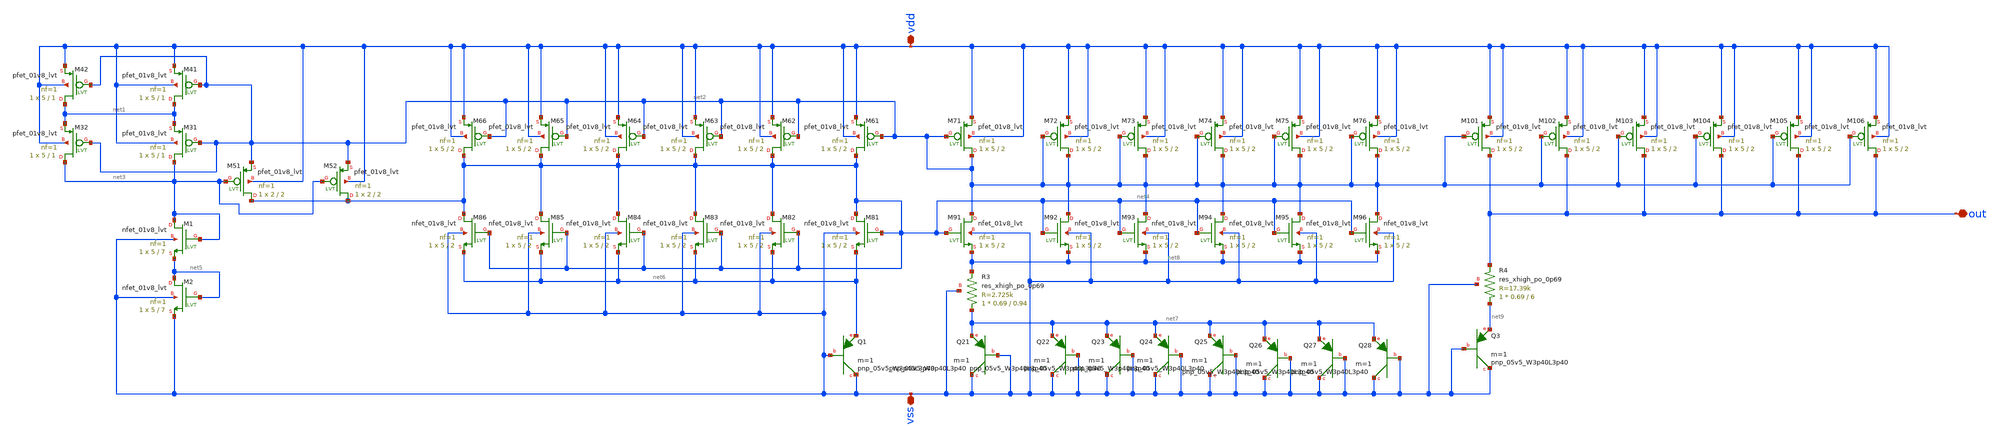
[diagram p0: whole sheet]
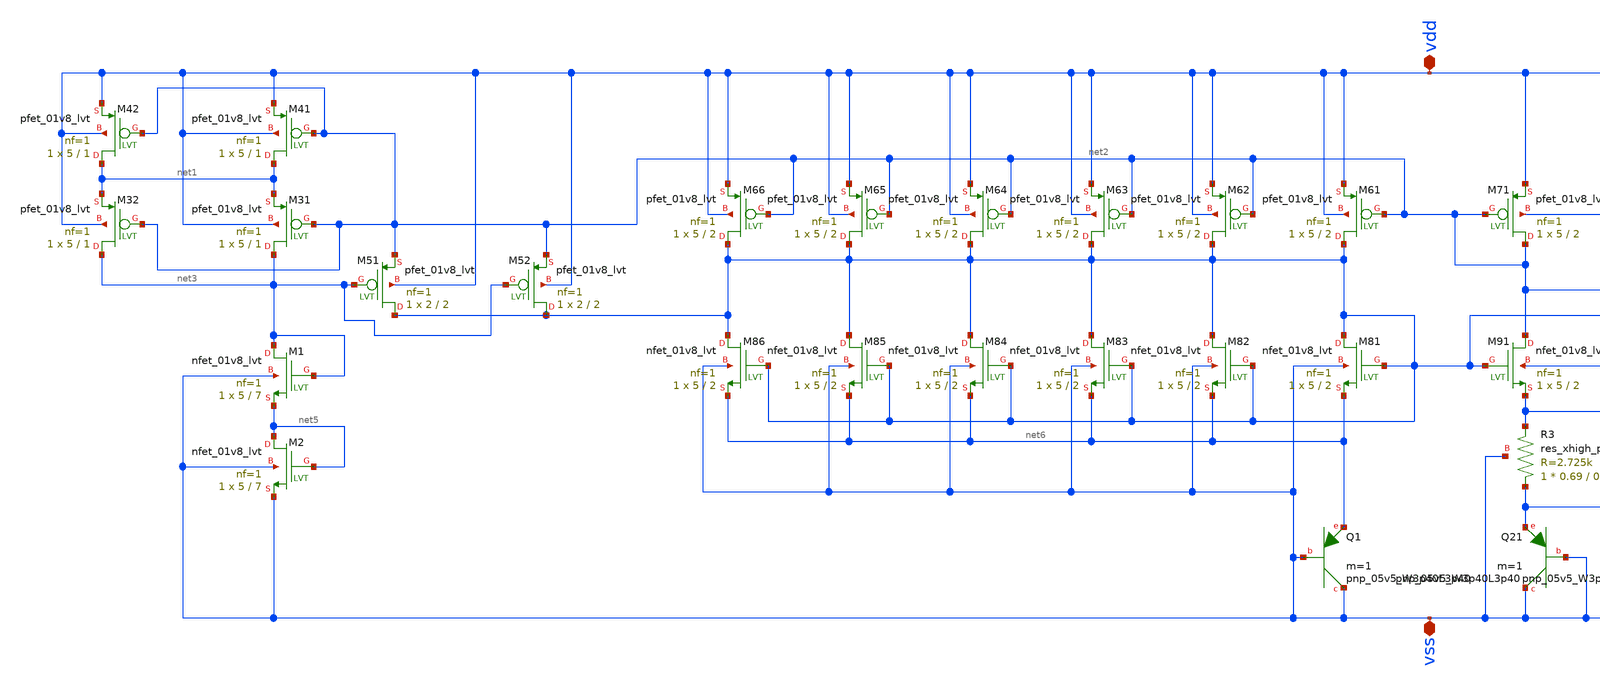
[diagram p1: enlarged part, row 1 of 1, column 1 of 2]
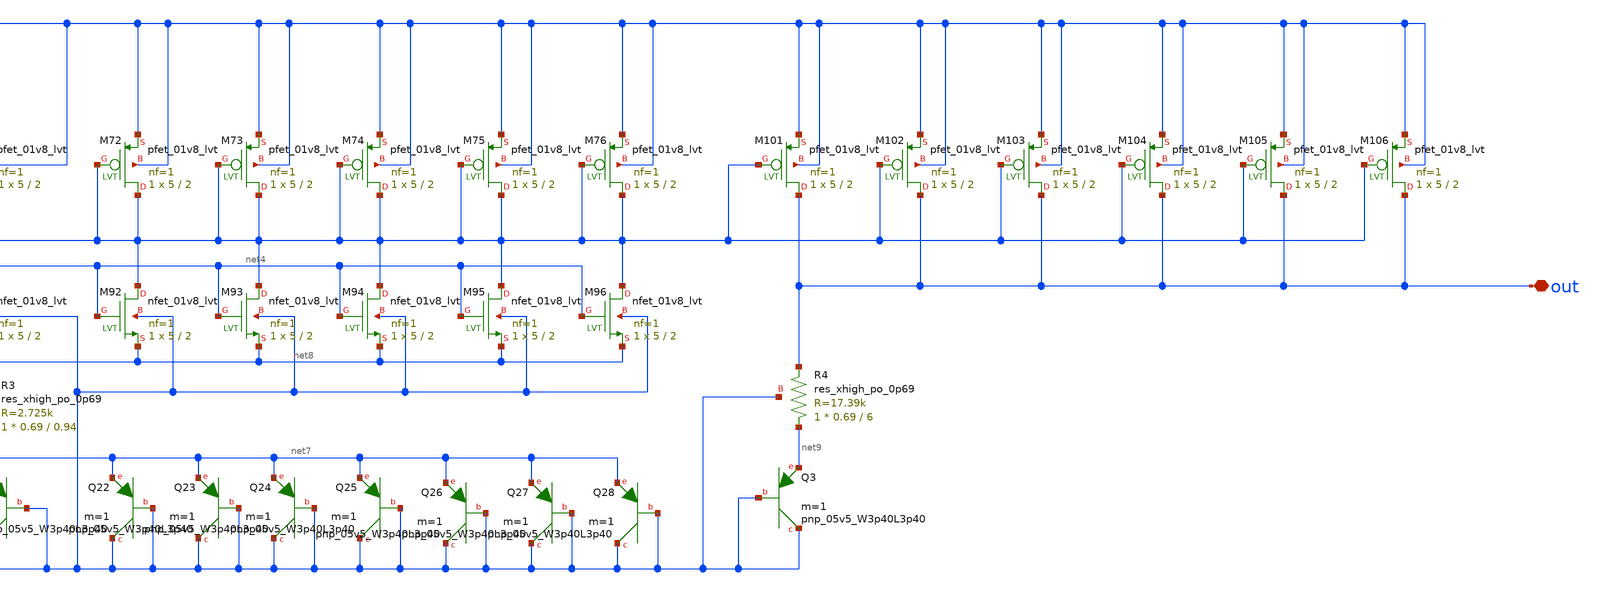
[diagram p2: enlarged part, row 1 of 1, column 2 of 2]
** sch_path: XSCHEM/For_Layout/BGR_lvt.sch
**.subckt BGR_lvt vdd vss out
*.iopin vdd
*.iopin vss
*.iopin out
XM1 net3 net3 net5 vss sky130_fd_pr__nfet_01v8_lvt L=7 W=5 nf=1 ad='int((nf+1)/2) * W/nf * 0.29' as='int((nf+2)/2) * W/nf * 0.29'
+ pd='2*int((nf+1)/2) * (W/nf + 0.29)' ps='2*int((nf+2)/2) * (W/nf + 0.29)' nrd='0.29 / W' nrs='0.29 / W'
+ sa=0 sb=0 sd=0 mult=1 m=1
XM2 net5 net5 vss vss sky130_fd_pr__nfet_01v8_lvt L=7 W=5 nf=1 ad='int((nf+1)/2) * W/nf * 0.29' as='int((nf+2)/2) * W/nf * 0.29'
+ pd='2*int((nf+1)/2) * (W/nf + 0.29)' ps='2*int((nf+2)/2) * (W/nf + 0.29)' nrd='0.29 / W' nrs='0.29 / W'
+ sa=0 sb=0 sd=0 mult=1 m=1
XM31 net3 net2 net1 vdd sky130_fd_pr__pfet_01v8_lvt L=1 W=5 nf=1 ad='int((nf+1)/2) * W/nf * 0.29' as='int((nf+2)/2) * W/nf * 0.29'
+ pd='2*int((nf+1)/2) * (W/nf + 0.29)' ps='2*int((nf+2)/2) * (W/nf + 0.29)' nrd='0.29 / W' nrs='0.29 / W'
+ sa=0 sb=0 sd=0 mult=1 m=1
XM41 net1 net2 vdd vdd sky130_fd_pr__pfet_01v8_lvt L=1 W=5 nf=1 ad='int((nf+1)/2) * W/nf * 0.29' as='int((nf+2)/2) * W/nf * 0.29'
+ pd='2*int((nf+1)/2) * (W/nf + 0.29)' ps='2*int((nf+2)/2) * (W/nf + 0.29)' nrd='0.29 / W' nrs='0.29 / W'
+ sa=0 sb=0 sd=0 mult=1 m=1
XM51 net4 net3 net2 vdd sky130_fd_pr__pfet_01v8_lvt L=2 W=2 nf=1 ad='int((nf+1)/2) * W/nf * 0.29' as='int((nf+2)/2) * W/nf * 0.29'
+ pd='2*int((nf+1)/2) * (W/nf + 0.29)' ps='2*int((nf+2)/2) * (W/nf + 0.29)' nrd='0.29 / W' nrs='0.29 / W'
+ sa=0 sb=0 sd=0 mult=1 m=1
XM61 net4 net2 vdd vdd sky130_fd_pr__pfet_01v8_lvt L=2 W=5 nf=1 ad='int((nf+1)/2) * W/nf * 0.29' as='int((nf+2)/2) * W/nf * 0.29'
+ pd='2*int((nf+1)/2) * (W/nf + 0.29)' ps='2*int((nf+2)/2) * (W/nf + 0.29)' nrd='0.29 / W' nrs='0.29 / W'
+ sa=0 sb=0 sd=0 mult=1 m=1
XM71 net2 net2 vdd vdd sky130_fd_pr__pfet_01v8_lvt L=2 W=5 nf=1 ad='int((nf+1)/2) * W/nf * 0.29' as='int((nf+2)/2) * W/nf * 0.29'
+ pd='2*int((nf+1)/2) * (W/nf + 0.29)' ps='2*int((nf+2)/2) * (W/nf + 0.29)' nrd='0.29 / W' nrs='0.29 / W'
+ sa=0 sb=0 sd=0 mult=1 m=1
XM81 net4 net4 net6 vss sky130_fd_pr__nfet_01v8_lvt L=2 W=5 nf=1 ad='int((nf+1)/2) * W/nf * 0.29' as='int((nf+2)/2) * W/nf * 0.29'
+ pd='2*int((nf+1)/2) * (W/nf + 0.29)' ps='2*int((nf+2)/2) * (W/nf + 0.29)' nrd='0.29 / W' nrs='0.29 / W'
+ sa=0 sb=0 sd=0 mult=1 m=1
XM91 net2 net4 net8 vss sky130_fd_pr__nfet_01v8_lvt L=2 W=5 nf=1 ad='int((nf+1)/2) * W/nf * 0.29' as='int((nf+2)/2) * W/nf * 0.29'
+ pd='2*int((nf+1)/2) * (W/nf + 0.29)' ps='2*int((nf+2)/2) * (W/nf + 0.29)' nrd='0.29 / W' nrs='0.29 / W'
+ sa=0 sb=0 sd=0 mult=1 m=1
XQ1 vss vss net6 sky130_fd_pr__pnp_05v5_W3p40L3p40 m=1
XQ21 vss vss net7 sky130_fd_pr__pnp_05v5_W3p40L3p40 m=1
XM101 out net2 vdd vdd sky130_fd_pr__pfet_01v8_lvt L=2 W=5 nf=1 ad='int((nf+1)/2) * W/nf * 0.29' as='int((nf+2)/2) * W/nf * 0.29'
+ pd='2*int((nf+1)/2) * (W/nf + 0.29)' ps='2*int((nf+2)/2) * (W/nf + 0.29)' nrd='0.29 / W' nrs='0.29 / W'
+ sa=0 sb=0 sd=0 mult=1 m=1
XQ3 vss vss net9 sky130_fd_pr__pnp_05v5_W3p40L3p40 m=1
XR3 net7 net8 vss sky130_fd_pr__res_xhigh_po_0p69 L=0.94 mult=1 m=1
XR4 net9 out vss sky130_fd_pr__res_xhigh_po_0p69 L=6 mult=1 m=1
XM42 net1 net2 vdd vdd sky130_fd_pr__pfet_01v8_lvt L=1 W=5 nf=1 ad='int((nf+1)/2) * W/nf * 0.29' as='int((nf+2)/2) * W/nf * 0.29'
+ pd='2*int((nf+1)/2) * (W/nf + 0.29)' ps='2*int((nf+2)/2) * (W/nf + 0.29)' nrd='0.29 / W' nrs='0.29 / W'
+ sa=0 sb=0 sd=0 mult=1 m=1
XM32 net3 net2 net1 vdd sky130_fd_pr__pfet_01v8_lvt L=1 W=5 nf=1 ad='int((nf+1)/2) * W/nf * 0.29' as='int((nf+2)/2) * W/nf * 0.29'
+ pd='2*int((nf+1)/2) * (W/nf + 0.29)' ps='2*int((nf+2)/2) * (W/nf + 0.29)' nrd='0.29 / W' nrs='0.29 / W'
+ sa=0 sb=0 sd=0 mult=1 m=1
XM52 net4 net3 net2 vdd sky130_fd_pr__pfet_01v8_lvt L=2 W=2 nf=1 ad='int((nf+1)/2) * W/nf * 0.29' as='int((nf+2)/2) * W/nf * 0.29'
+ pd='2*int((nf+1)/2) * (W/nf + 0.29)' ps='2*int((nf+2)/2) * (W/nf + 0.29)' nrd='0.29 / W' nrs='0.29 / W'
+ sa=0 sb=0 sd=0 mult=1 m=1
XM62 net4 net2 vdd vdd sky130_fd_pr__pfet_01v8_lvt L=2 W=5 nf=1 ad='int((nf+1)/2) * W/nf * 0.29' as='int((nf+2)/2) * W/nf * 0.29'
+ pd='2*int((nf+1)/2) * (W/nf + 0.29)' ps='2*int((nf+2)/2) * (W/nf + 0.29)' nrd='0.29 / W' nrs='0.29 / W'
+ sa=0 sb=0 sd=0 mult=1 m=1
XM63 net4 net2 vdd vdd sky130_fd_pr__pfet_01v8_lvt L=2 W=5 nf=1 ad='int((nf+1)/2) * W/nf * 0.29' as='int((nf+2)/2) * W/nf * 0.29'
+ pd='2*int((nf+1)/2) * (W/nf + 0.29)' ps='2*int((nf+2)/2) * (W/nf + 0.29)' nrd='0.29 / W' nrs='0.29 / W'
+ sa=0 sb=0 sd=0 mult=1 m=1
XM64 net4 net2 vdd vdd sky130_fd_pr__pfet_01v8_lvt L=2 W=5 nf=1 ad='int((nf+1)/2) * W/nf * 0.29' as='int((nf+2)/2) * W/nf * 0.29'
+ pd='2*int((nf+1)/2) * (W/nf + 0.29)' ps='2*int((nf+2)/2) * (W/nf + 0.29)' nrd='0.29 / W' nrs='0.29 / W'
+ sa=0 sb=0 sd=0 mult=1 m=1
XM65 net4 net2 vdd vdd sky130_fd_pr__pfet_01v8_lvt L=2 W=5 nf=1 ad='int((nf+1)/2) * W/nf * 0.29' as='int((nf+2)/2) * W/nf * 0.29'
+ pd='2*int((nf+1)/2) * (W/nf + 0.29)' ps='2*int((nf+2)/2) * (W/nf + 0.29)' nrd='0.29 / W' nrs='0.29 / W'
+ sa=0 sb=0 sd=0 mult=1 m=1
XM66 net4 net2 vdd vdd sky130_fd_pr__pfet_01v8_lvt L=2 W=5 nf=1 ad='int((nf+1)/2) * W/nf * 0.29' as='int((nf+2)/2) * W/nf * 0.29'
+ pd='2*int((nf+1)/2) * (W/nf + 0.29)' ps='2*int((nf+2)/2) * (W/nf + 0.29)' nrd='0.29 / W' nrs='0.29 / W'
+ sa=0 sb=0 sd=0 mult=1 m=1
XM82 net4 net4 net6 vss sky130_fd_pr__nfet_01v8_lvt L=2 W=5 nf=1 ad='int((nf+1)/2) * W/nf * 0.29' as='int((nf+2)/2) * W/nf * 0.29'
+ pd='2*int((nf+1)/2) * (W/nf + 0.29)' ps='2*int((nf+2)/2) * (W/nf + 0.29)' nrd='0.29 / W' nrs='0.29 / W'
+ sa=0 sb=0 sd=0 mult=1 m=1
XM83 net4 net4 net6 vss sky130_fd_pr__nfet_01v8_lvt L=2 W=5 nf=1 ad='int((nf+1)/2) * W/nf * 0.29' as='int((nf+2)/2) * W/nf * 0.29'
+ pd='2*int((nf+1)/2) * (W/nf + 0.29)' ps='2*int((nf+2)/2) * (W/nf + 0.29)' nrd='0.29 / W' nrs='0.29 / W'
+ sa=0 sb=0 sd=0 mult=1 m=1
XM84 net4 net4 net6 vss sky130_fd_pr__nfet_01v8_lvt L=2 W=5 nf=1 ad='int((nf+1)/2) * W/nf * 0.29' as='int((nf+2)/2) * W/nf * 0.29'
+ pd='2*int((nf+1)/2) * (W/nf + 0.29)' ps='2*int((nf+2)/2) * (W/nf + 0.29)' nrd='0.29 / W' nrs='0.29 / W'
+ sa=0 sb=0 sd=0 mult=1 m=1
XM85 net4 net4 net6 vss sky130_fd_pr__nfet_01v8_lvt L=2 W=5 nf=1 ad='int((nf+1)/2) * W/nf * 0.29' as='int((nf+2)/2) * W/nf * 0.29'
+ pd='2*int((nf+1)/2) * (W/nf + 0.29)' ps='2*int((nf+2)/2) * (W/nf + 0.29)' nrd='0.29 / W' nrs='0.29 / W'
+ sa=0 sb=0 sd=0 mult=1 m=1
XM86 net4 net4 net6 vss sky130_fd_pr__nfet_01v8_lvt L=2 W=5 nf=1 ad='int((nf+1)/2) * W/nf * 0.29' as='int((nf+2)/2) * W/nf * 0.29'
+ pd='2*int((nf+1)/2) * (W/nf + 0.29)' ps='2*int((nf+2)/2) * (W/nf + 0.29)' nrd='0.29 / W' nrs='0.29 / W'
+ sa=0 sb=0 sd=0 mult=1 m=1
XM72 net2 net2 vdd vdd sky130_fd_pr__pfet_01v8_lvt L=2 W=5 nf=1 ad='int((nf+1)/2) * W/nf * 0.29' as='int((nf+2)/2) * W/nf * 0.29'
+ pd='2*int((nf+1)/2) * (W/nf + 0.29)' ps='2*int((nf+2)/2) * (W/nf + 0.29)' nrd='0.29 / W' nrs='0.29 / W'
+ sa=0 sb=0 sd=0 mult=1 m=1
XM73 net2 net2 vdd vdd sky130_fd_pr__pfet_01v8_lvt L=2 W=5 nf=1 ad='int((nf+1)/2) * W/nf * 0.29' as='int((nf+2)/2) * W/nf * 0.29'
+ pd='2*int((nf+1)/2) * (W/nf + 0.29)' ps='2*int((nf+2)/2) * (W/nf + 0.29)' nrd='0.29 / W' nrs='0.29 / W'
+ sa=0 sb=0 sd=0 mult=1 m=1
XM74 net2 net2 vdd vdd sky130_fd_pr__pfet_01v8_lvt L=2 W=5 nf=1 ad='int((nf+1)/2) * W/nf * 0.29' as='int((nf+2)/2) * W/nf * 0.29'
+ pd='2*int((nf+1)/2) * (W/nf + 0.29)' ps='2*int((nf+2)/2) * (W/nf + 0.29)' nrd='0.29 / W' nrs='0.29 / W'
+ sa=0 sb=0 sd=0 mult=1 m=1
XM75 net2 net2 vdd vdd sky130_fd_pr__pfet_01v8_lvt L=2 W=5 nf=1 ad='int((nf+1)/2) * W/nf * 0.29' as='int((nf+2)/2) * W/nf * 0.29'
+ pd='2*int((nf+1)/2) * (W/nf + 0.29)' ps='2*int((nf+2)/2) * (W/nf + 0.29)' nrd='0.29 / W' nrs='0.29 / W'
+ sa=0 sb=0 sd=0 mult=1 m=1
XM76 net2 net2 vdd vdd sky130_fd_pr__pfet_01v8_lvt L=2 W=5 nf=1 ad='int((nf+1)/2) * W/nf * 0.29' as='int((nf+2)/2) * W/nf * 0.29'
+ pd='2*int((nf+1)/2) * (W/nf + 0.29)' ps='2*int((nf+2)/2) * (W/nf + 0.29)' nrd='0.29 / W' nrs='0.29 / W'
+ sa=0 sb=0 sd=0 mult=1 m=1
XM92 net2 net4 net8 vss sky130_fd_pr__nfet_01v8_lvt L=2 W=5 nf=1 ad='int((nf+1)/2) * W/nf * 0.29' as='int((nf+2)/2) * W/nf * 0.29'
+ pd='2*int((nf+1)/2) * (W/nf + 0.29)' ps='2*int((nf+2)/2) * (W/nf + 0.29)' nrd='0.29 / W' nrs='0.29 / W'
+ sa=0 sb=0 sd=0 mult=1 m=1
XM93 net2 net4 net8 vss sky130_fd_pr__nfet_01v8_lvt L=2 W=5 nf=1 ad='int((nf+1)/2) * W/nf * 0.29' as='int((nf+2)/2) * W/nf * 0.29'
+ pd='2*int((nf+1)/2) * (W/nf + 0.29)' ps='2*int((nf+2)/2) * (W/nf + 0.29)' nrd='0.29 / W' nrs='0.29 / W'
+ sa=0 sb=0 sd=0 mult=1 m=1
XM94 net2 net4 net8 vss sky130_fd_pr__nfet_01v8_lvt L=2 W=5 nf=1 ad='int((nf+1)/2) * W/nf * 0.29' as='int((nf+2)/2) * W/nf * 0.29'
+ pd='2*int((nf+1)/2) * (W/nf + 0.29)' ps='2*int((nf+2)/2) * (W/nf + 0.29)' nrd='0.29 / W' nrs='0.29 / W'
+ sa=0 sb=0 sd=0 mult=1 m=1
XM95 net2 net4 net8 vss sky130_fd_pr__nfet_01v8_lvt L=2 W=5 nf=1 ad='int((nf+1)/2) * W/nf * 0.29' as='int((nf+2)/2) * W/nf * 0.29'
+ pd='2*int((nf+1)/2) * (W/nf + 0.29)' ps='2*int((nf+2)/2) * (W/nf + 0.29)' nrd='0.29 / W' nrs='0.29 / W'
+ sa=0 sb=0 sd=0 mult=1 m=1
XM96 net2 net4 net8 vss sky130_fd_pr__nfet_01v8_lvt L=2 W=5 nf=1 ad='int((nf+1)/2) * W/nf * 0.29' as='int((nf+2)/2) * W/nf * 0.29'
+ pd='2*int((nf+1)/2) * (W/nf + 0.29)' ps='2*int((nf+2)/2) * (W/nf + 0.29)' nrd='0.29 / W' nrs='0.29 / W'
+ sa=0 sb=0 sd=0 mult=1 m=1
XM102 out net2 vdd vdd sky130_fd_pr__pfet_01v8_lvt L=2 W=5 nf=1 ad='int((nf+1)/2) * W/nf * 0.29' as='int((nf+2)/2) * W/nf * 0.29'
+ pd='2*int((nf+1)/2) * (W/nf + 0.29)' ps='2*int((nf+2)/2) * (W/nf + 0.29)' nrd='0.29 / W' nrs='0.29 / W'
+ sa=0 sb=0 sd=0 mult=1 m=1
XM103 out net2 vdd vdd sky130_fd_pr__pfet_01v8_lvt L=2 W=5 nf=1 ad='int((nf+1)/2) * W/nf * 0.29' as='int((nf+2)/2) * W/nf * 0.29'
+ pd='2*int((nf+1)/2) * (W/nf + 0.29)' ps='2*int((nf+2)/2) * (W/nf + 0.29)' nrd='0.29 / W' nrs='0.29 / W'
+ sa=0 sb=0 sd=0 mult=1 m=1
XM104 out net2 vdd vdd sky130_fd_pr__pfet_01v8_lvt L=2 W=5 nf=1 ad='int((nf+1)/2) * W/nf * 0.29' as='int((nf+2)/2) * W/nf * 0.29'
+ pd='2*int((nf+1)/2) * (W/nf + 0.29)' ps='2*int((nf+2)/2) * (W/nf + 0.29)' nrd='0.29 / W' nrs='0.29 / W'
+ sa=0 sb=0 sd=0 mult=1 m=1
XM105 out net2 vdd vdd sky130_fd_pr__pfet_01v8_lvt L=2 W=5 nf=1 ad='int((nf+1)/2) * W/nf * 0.29' as='int((nf+2)/2) * W/nf * 0.29'
+ pd='2*int((nf+1)/2) * (W/nf + 0.29)' ps='2*int((nf+2)/2) * (W/nf + 0.29)' nrd='0.29 / W' nrs='0.29 / W'
+ sa=0 sb=0 sd=0 mult=1 m=1
XM106 out net2 vdd vdd sky130_fd_pr__pfet_01v8_lvt L=2 W=5 nf=1 ad='int((nf+1)/2) * W/nf * 0.29' as='int((nf+2)/2) * W/nf * 0.29'
+ pd='2*int((nf+1)/2) * (W/nf + 0.29)' ps='2*int((nf+2)/2) * (W/nf + 0.29)' nrd='0.29 / W' nrs='0.29 / W'
+ sa=0 sb=0 sd=0 mult=1 m=1
XQ22 vss vss net7 sky130_fd_pr__pnp_05v5_W3p40L3p40 m=1
XQ23 vss vss net7 sky130_fd_pr__pnp_05v5_W3p40L3p40 m=1
XQ24 vss vss net7 sky130_fd_pr__pnp_05v5_W3p40L3p40 m=1
XQ25 vss vss net7 sky130_fd_pr__pnp_05v5_W3p40L3p40 m=1
XQ26 vss vss net7 sky130_fd_pr__pnp_05v5_W3p40L3p40 m=1
XQ27 vss vss net7 sky130_fd_pr__pnp_05v5_W3p40L3p40 m=1
XQ28 vss vss net7 sky130_fd_pr__pnp_05v5_W3p40L3p40 m=1
**.ends
.end
